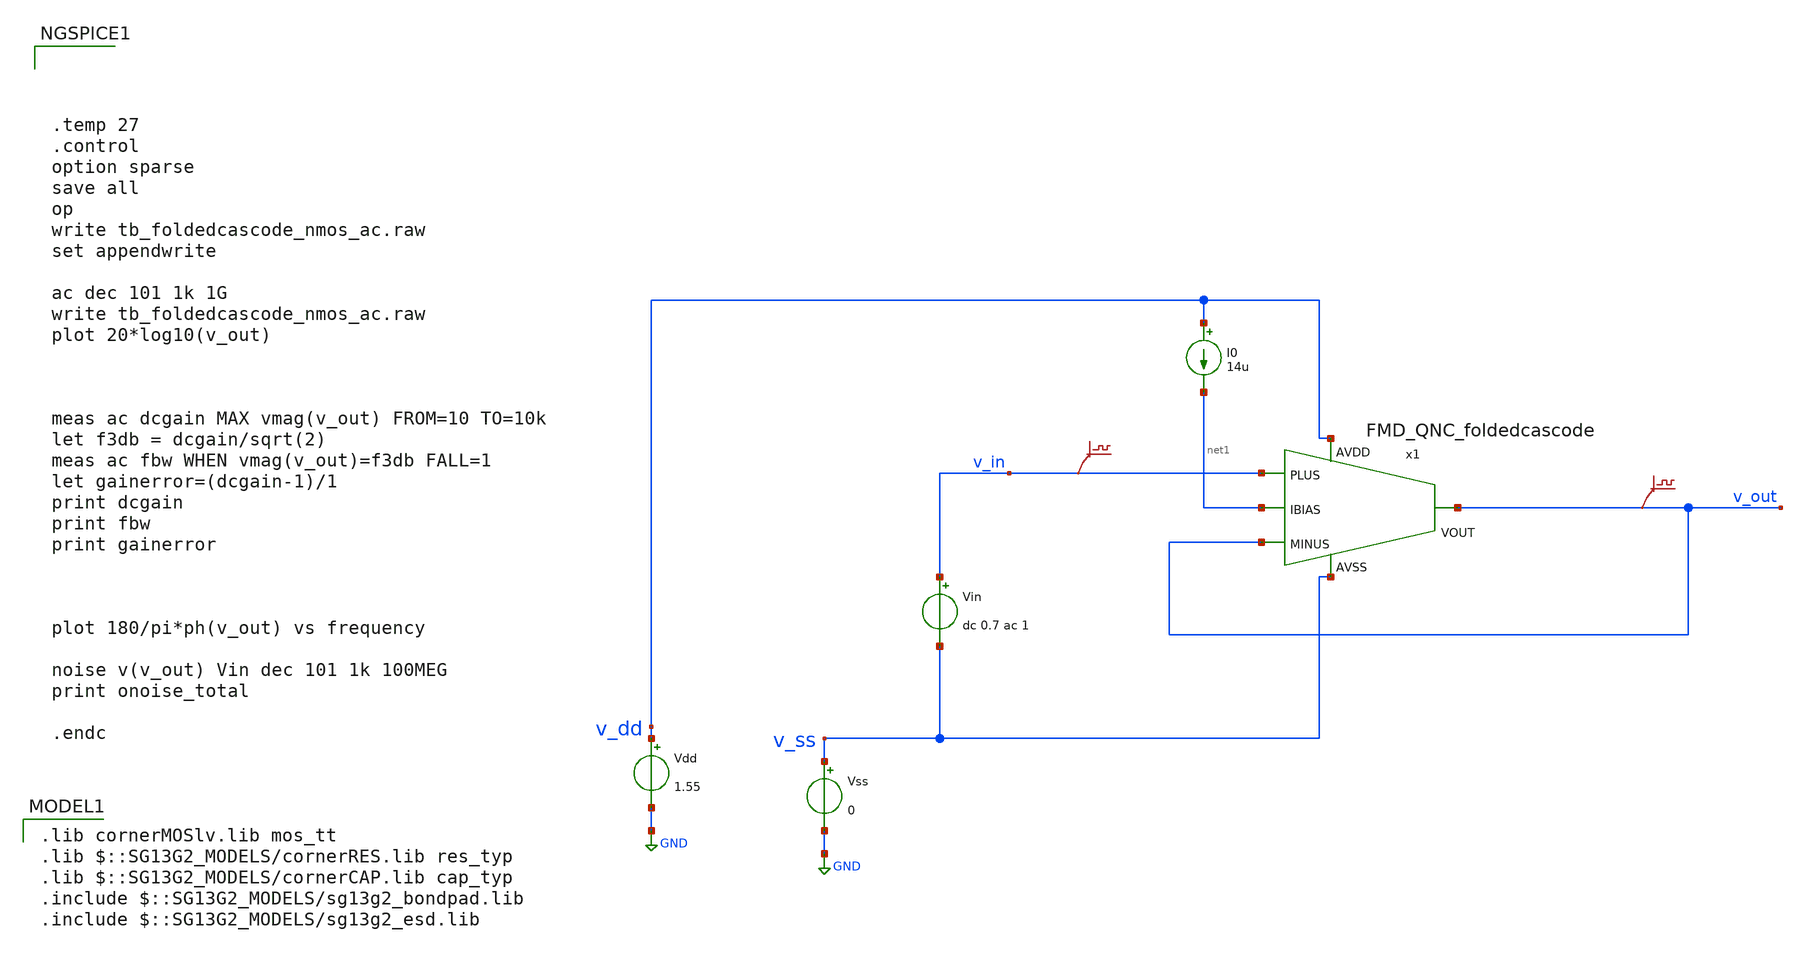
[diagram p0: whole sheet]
** sch_path: Designs/final_tapeout_submissions/OTALED/1_schematics/FMD_QNC_foldedcascode_ac.sch
* (c) 2025 Thesis_HP, Apache-2.0 license
**.subckt FMD_QNC_foldedcascode_ac
Vss v_ss GND 0
Vdd v_dd GND 1.55
Vin v_in v_ss dc 0.7 ac 1
.save v(v_in)
I0 v_dd net1 14u
.save v(v_out)
x1 v_dd net1 v_in v_out v_out v_ss FMD_QNC_foldedcascode
**** begin user architecture code




.temp 27
.control
option sparse
save all
op
write tb_foldedcascode_nmos_ac.raw
set appendwrite

ac dec 101 1k 1G
write tb_foldedcascode_nmos_ac.raw
plot 20*log10(v_out)



meas ac dcgain MAX vmag(v_out) FROM=10 TO=10k
let f3db = dcgain/sqrt(2)
meas ac fbw WHEN vmag(v_out)=f3db FALL=1
let gainerror=(dcgain-1)/1
print dcgain
print fbw
print gainerror



plot 180/pi*ph(v_out) vs frequency

noise v(v_out) Vin dec 101 1k 100MEG
print onoise_total

.endc


 .lib cornerMOSlv.lib mos_tt
.lib $::SG13G2_MODELS/cornerRES.lib res_typ
.lib $::SG13G2_MODELS/cornerCAP.lib cap_typ
.include $::SG13G2_MODELS/sg13g2_bondpad.lib
.include $::SG13G2_MODELS/sg13g2_esd.lib

**** end user architecture code
**.ends

* expanding   symbol:
*+  /foss/designs/thesis/TO_July2025_OTALED/OTALED/design_data/xschem/FMD_QNC_foldedcascode.sym # of pins=6
** sym_path: Designs/final_tapeout_submissions/OTALED/1_schematics/FMD_QNC_foldedcascode.sym
** sch_path: Designs/final_tapeout_submissions/OTALED/1_schematics/FMD_QNC_foldedcascode.sch
.subckt FMD_QNC_foldedcascode AVDD IBIAS PLUS MINUS VOUT AVSS
*.ipin PLUS
*.ipin MINUS
*.ipin AVSS
*.ipin IBIAS
*.ipin AVDD
*.opin VOUT
XM1 net6 MINUS net1 AVDD sg13_lv_pmos w=20u l=2u ng=4 m=1 mm_ok=1
XM5 net7 net8 net4 AVSS sg13_lv_nmos w=2u l=2u ng=2 m=1 mm_ok=1
XM2 net4 PLUS net1 AVDD sg13_lv_pmos w=20u l=2u ng=4 m=1 mm_ok=1
XM3 net2 net7 AVDD AVDD sg13_lv_pmos w=13u l=2u ng=2 m=1 mm_ok=1
XM4 net3 net7 AVDD AVDD sg13_lv_pmos w=13u l=2u ng=2 m=1 mm_ok=1
XM7 net7 net9 net2 AVDD sg13_lv_pmos w=8u l=2u ng=4 m=1 mm_ok=1
XM8 VOUT net9 net3 AVDD sg13_lv_pmos w=8u l=2u ng=4 m=1 mm_ok=1
XM6 VOUT net8 net6 AVSS sg13_lv_nmos w=2u l=2u ng=2 m=1 mm_ok=1
XM9 net4 net5 AVSS AVSS sg13_lv_nmos w=4u l=2u ng=2 m=1 mm_ok=1
XM0 net6 net5 AVSS AVSS sg13_lv_nmos w=4u l=2u ng=2 m=1 mm_ok=1
XMt net1 net10 AVDD AVDD sg13_lv_pmos w=32u l=5u ng=4 m=1 mm_ok=1
XM13 IBIAS net7 net5 AVSS sg13_lv_nmos w=4u l=2u ng=2 m=1 mm_ok=1
XM15 net5 net5 AVSS AVSS sg13_lv_nmos w=4u l=2u ng=1 m=1 mm_ok=1
XM16 net8 net5 AVSS AVSS sg13_lv_nmos w=4u l=2u ng=1 m=1 mm_ok=1
XM14 AVDD net7 net8 AVSS sg13_lv_nmos w=15u l=0.5u ng=2 m=1 mm_ok=1
XM12 net9 net8 AVSS AVSS sg13_lv_nmos w=2u l=2u ng=1 m=1 mm_ok=1
XM10 net9 net9 AVDD AVDD sg13_lv_pmos w=8u l=2u ng=2 m=1 mm_ok=1
XM11 net10 net5 AVSS AVSS sg13_lv_nmos w=4u l=2u ng=1 m=1 mm_ok=1
XMtb net10 net10 AVDD AVDD sg13_lv_pmos w=28u l=5u ng=4 m=1 mm_ok=1
XM18 net5 AVSS AVSS AVSS sg13_lv_nmos w=4u l=2u ng=1 m=1 mm_ok=1
XM19 AVDD AVSS AVSS AVSS sg13_lv_nmos w=15u l=0.5u ng=2 m=1 mm_ok=1
XM20 net4 AVSS AVSS AVSS sg13_lv_nmos w=4u l=2u ng=2 m=1 mm_ok=1
XM21 net7 AVSS AVSS AVSS sg13_lv_nmos w=2u l=2u ng=2 m=1 mm_ok=1
XM22 VOUT AVSS AVSS AVSS sg13_lv_nmos w=2u l=2u ng=2 m=1 mm_ok=1
XM23 AVDD AVDD net1 AVDD sg13_lv_pmos w=10u l=2u ng=2 m=1 mm_ok=1
XM24 AVDD AVDD net1 AVDD sg13_lv_pmos w=10u l=2u ng=2 m=1 mm_ok=1
XM25 net10 AVSS AVSS AVSS sg13_lv_nmos w=8u l=2u ng=2 m=1 mm_ok=1
XM26 net9 AVSS AVSS AVSS sg13_lv_nmos w=4u l=2u ng=2 m=1 mm_ok=1
XMtb1 net10 AVDD AVDD AVDD sg13_lv_pmos w=14u l=5u ng=2 m=1 mm_ok=1
XM27 net9 AVDD AVDD AVDD sg13_lv_pmos w=8u l=2u ng=2 m=1 mm_ok=1
XMt1 net1 AVDD AVDD AVDD sg13_lv_pmos w=16u l=5u ng=2 m=1 mm_ok=1
XD3 AVDD AVDD AVSS diodevdd_2kv m=1
XD4 AVDD AVDD AVSS diodevss_2kv m=1
XD5 AVDD AVSS AVSS diodevdd_2kv m=1
XD6 AVDD AVSS AVSS diodevss_2kv m=1
XX2 AVSS bondpad size=80u shape=0 padtype=0
XX3 AVDD bondpad size=80u shape=0 padtype=0
XD7 AVDD IBIAS AVSS diodevdd_2kv m=1
XD8 AVDD IBIAS AVSS diodevss_2kv m=1
XX4 IBIAS bondpad size=80u shape=0 padtype=0
XC2 VOUT AVSS cap_cmim w=25.82e-6 l=25.82e-6 m=1 mm_ok=1
XX1 VOUT bondpad size=80u shape=0 padtype=0
XX5 PLUS bondpad size=80u shape=0 padtype=0
XX6 MINUS bondpad size=80u shape=0 padtype=0
XM30 net8 AVSS AVSS AVSS sg13_lv_nmos w=4u l=2u ng=1 m=1 mm_ok=1
.ends

.GLOBAL GND
.end
